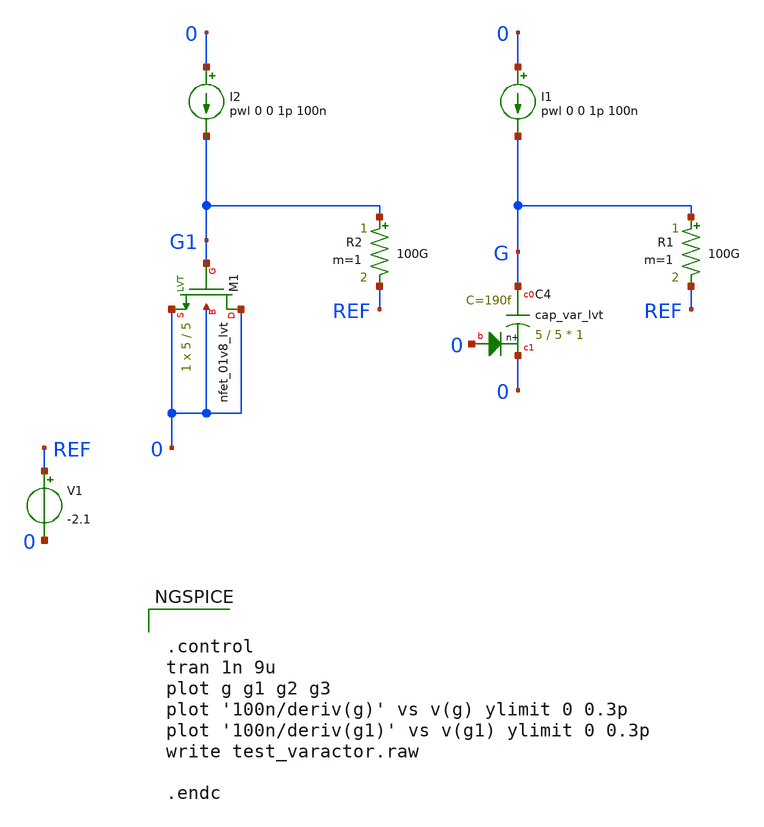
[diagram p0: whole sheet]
** sch_path: sky130_tests/test_varactor.sch
* Copyright 2021 Stefan Frederik Schippers
* Licensed under the Apache License, Version 2.0 (the "License");
* you may not use this file except in compliance with the License.
* You may obtain a copy of the License at
* https://www.apache.org/licenses/LICENSE-2.0
* Unless required by applicable law or agreed to in writing, software
* distributed under the License is distributed on an "AS IS" BASIS,
* WITHOUT WARRANTIES OR CONDITIONS OF ANY KIND, either express or implied.
* See the License for the specific language governing permissions and
* limitations under the License.
**.subckt test_varactor
I1 0 G pwl 0 0 1p 100n
R1 G REF 100G m=1
I2 0 G1 pwl 0 0 1p 100n
R2 G1 REF 100G m=1
V1 REF 0 -2.1
XM1 0 G1 0 sky130_fd_pr__nfet_01v8_lvt W=5 L=5 ad='W * 0.29' pd='2 * (W + 0.29)' as='W * 0.29' ps='2 * (W + 0.29)'
+ nrd='0.29 / W' nrs='0.29 / W' sa=0 sb=0 sd=0 nf=1 mult=1 m=1
XC4 G 0 0 sky130_fd_pr__cap_var_lvt W=5 L=5 VM=1 m=1
**** begin user architecture code


.control
tran 1n 9u
plot g g1 g2 g3
plot '100n/deriv(g)' vs v(g) ylimit 0 0.3p
plot '100n/deriv(g1)' vs v(g1) ylimit 0 0.3p
write test_varactor.raw

.endc



** opencircuitdesign pdks install
.lib $::SKYWATER_MODELS/sky130.lib.spice tt


**** end user architecture code
**.ends
.end
